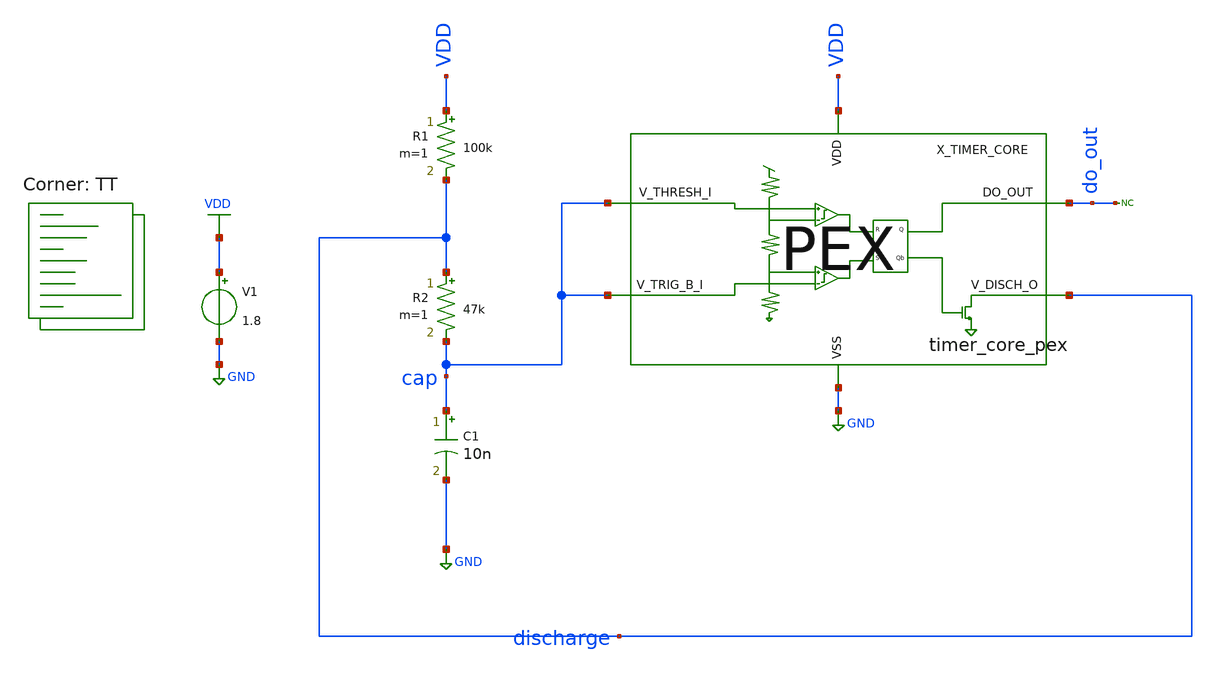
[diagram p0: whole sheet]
** sch_path: xsch/tb/timer_core/tb_pex_timer_core_astable.sch
**.subckt tb_pex_timer_core_astable
V1 VDD GND 1.8
R1 VDD discharge 100k m=1
R2 discharge cap 47k m=1
C1 cap GND 10n m=1
* noconn do_out
X_TIMER_CORE cap discharge do_out GND VDD cap timer_core_pex
**** begin user architecture code


.ic v(cap) = 0

.control
	tran 0.1u 10m
	;plot v(cap) v(discharge) v(do_out)

	;plot v(x_timer_core.v0p6) v(x_timer_core.v1p2) v(x_timer_core.bias_p) v(x_timer_core.bias_1)
+ v(x_timer_core.bias_2) v(x_timer_core.bias_3) v(x_timer_core.bias_n)

	;plot v(x_timer_core.sr_r) v(x_timer_core.sr_s) v(x_timer_core.v1p2) v(x_timer_core.v0p6)
	;plot v(x_timer_core.bias_n) v(x_timer_core.bias_1) v(x_timer_core.bias_2) v(x_timer_core.bias_3)
+ v(x_timer_core.bias_p)
	plot v(x_timer_core.sr_r) v(x_timer_core.sr_s)

	plot v(x_timer_core.x_comp_p_top/latch_left) v(x_timer_core.x_comp_p_top/latch_right)
+ v(x_timer_core.x_comp_p_top/tail) v(x_timer_core.x_comp_p_top/out_left)
.endc
.end


.lib $::SKYWATER_MODELS/sky130.lib.spice TT


.save all
.save v(do_out) v(discharge) v(cap) v(x_timer_core.out_inv3) v(cap2)

.savecurrents




.include ~/projects/tt06_555/xsch/ip/timers/timer_core/timer_core_pex.spice


**** end user architecture code
**.ends
.GLOBAL VDD
.GLOBAL GND
.end
